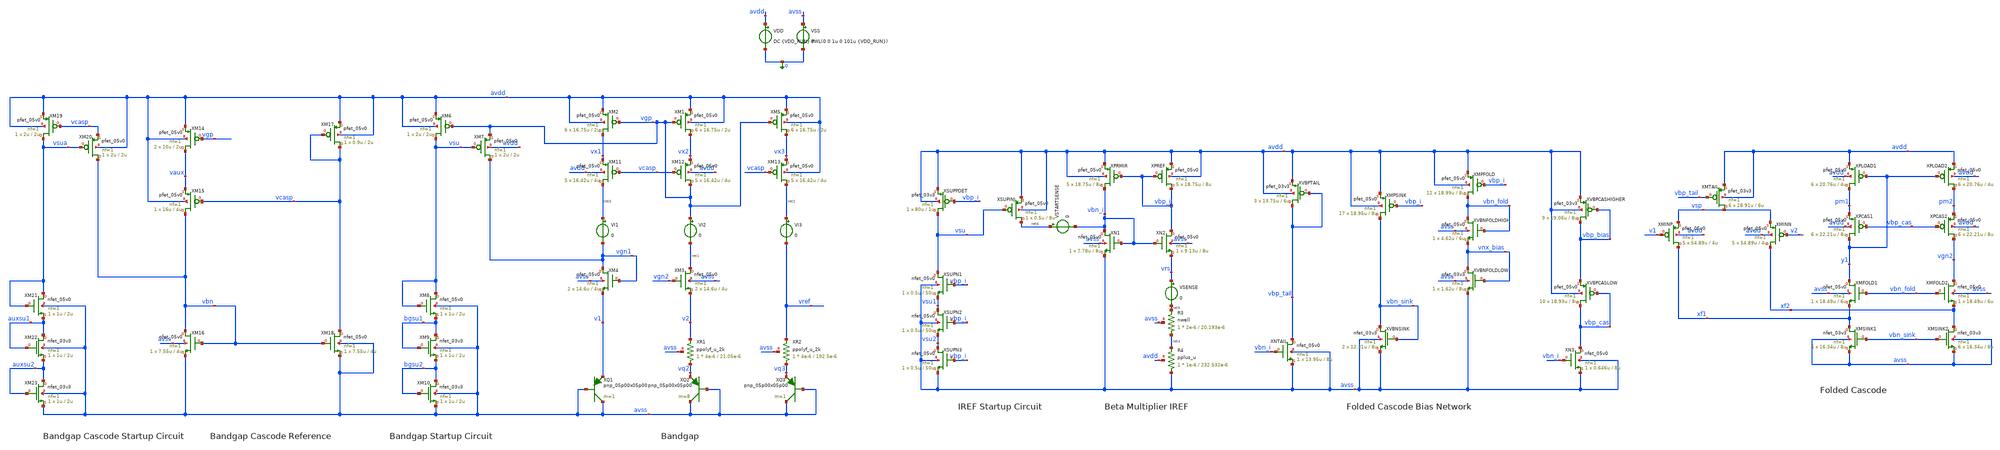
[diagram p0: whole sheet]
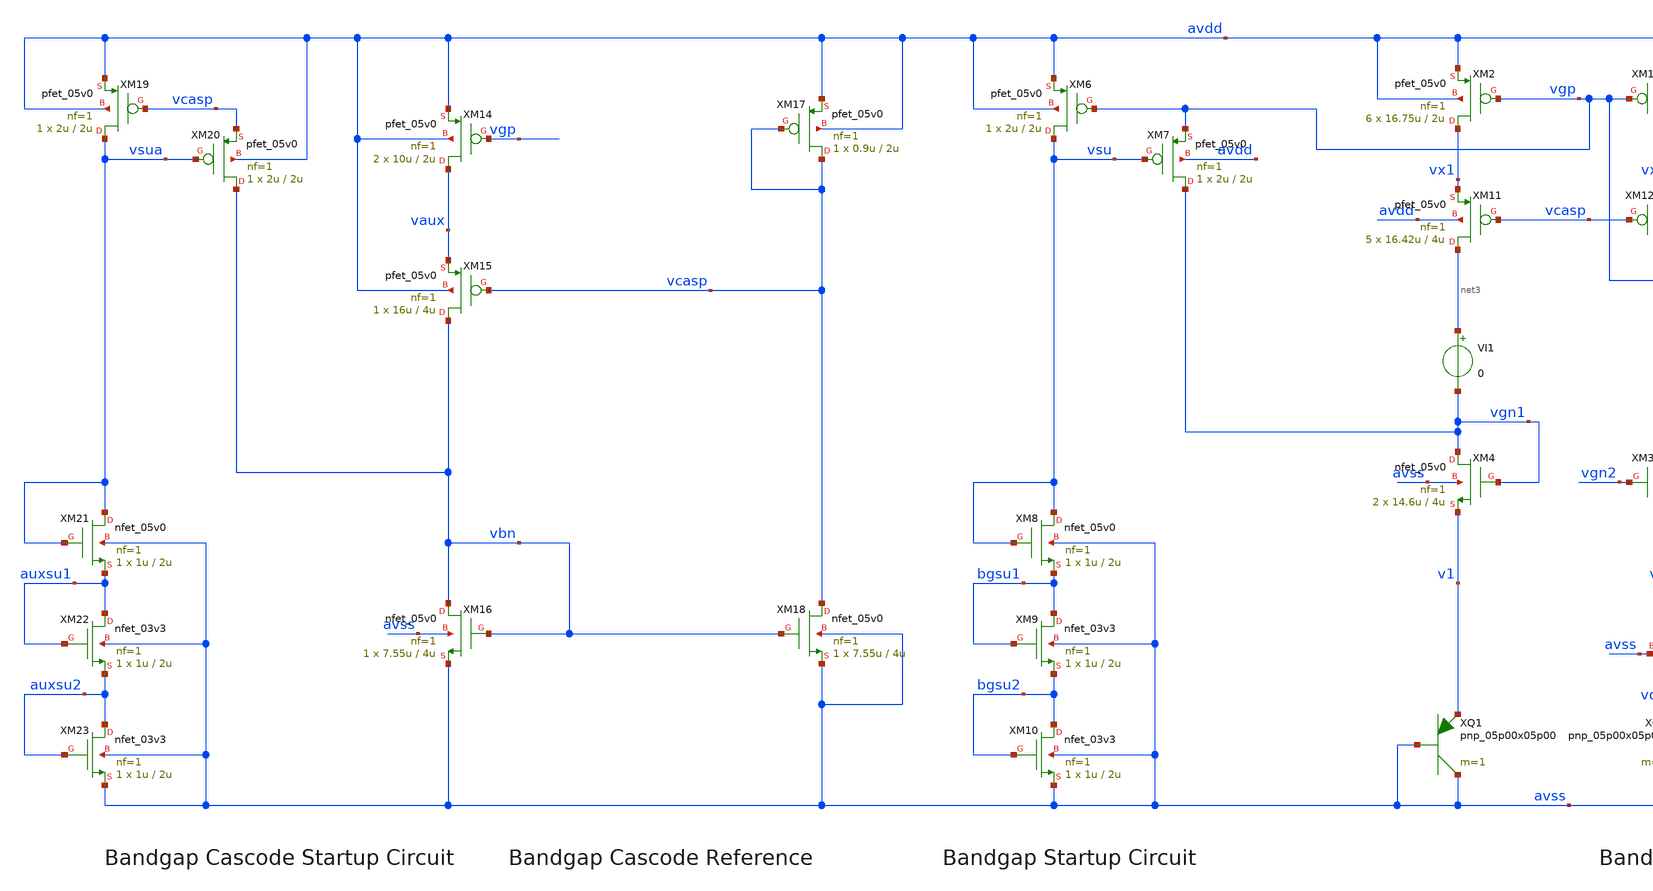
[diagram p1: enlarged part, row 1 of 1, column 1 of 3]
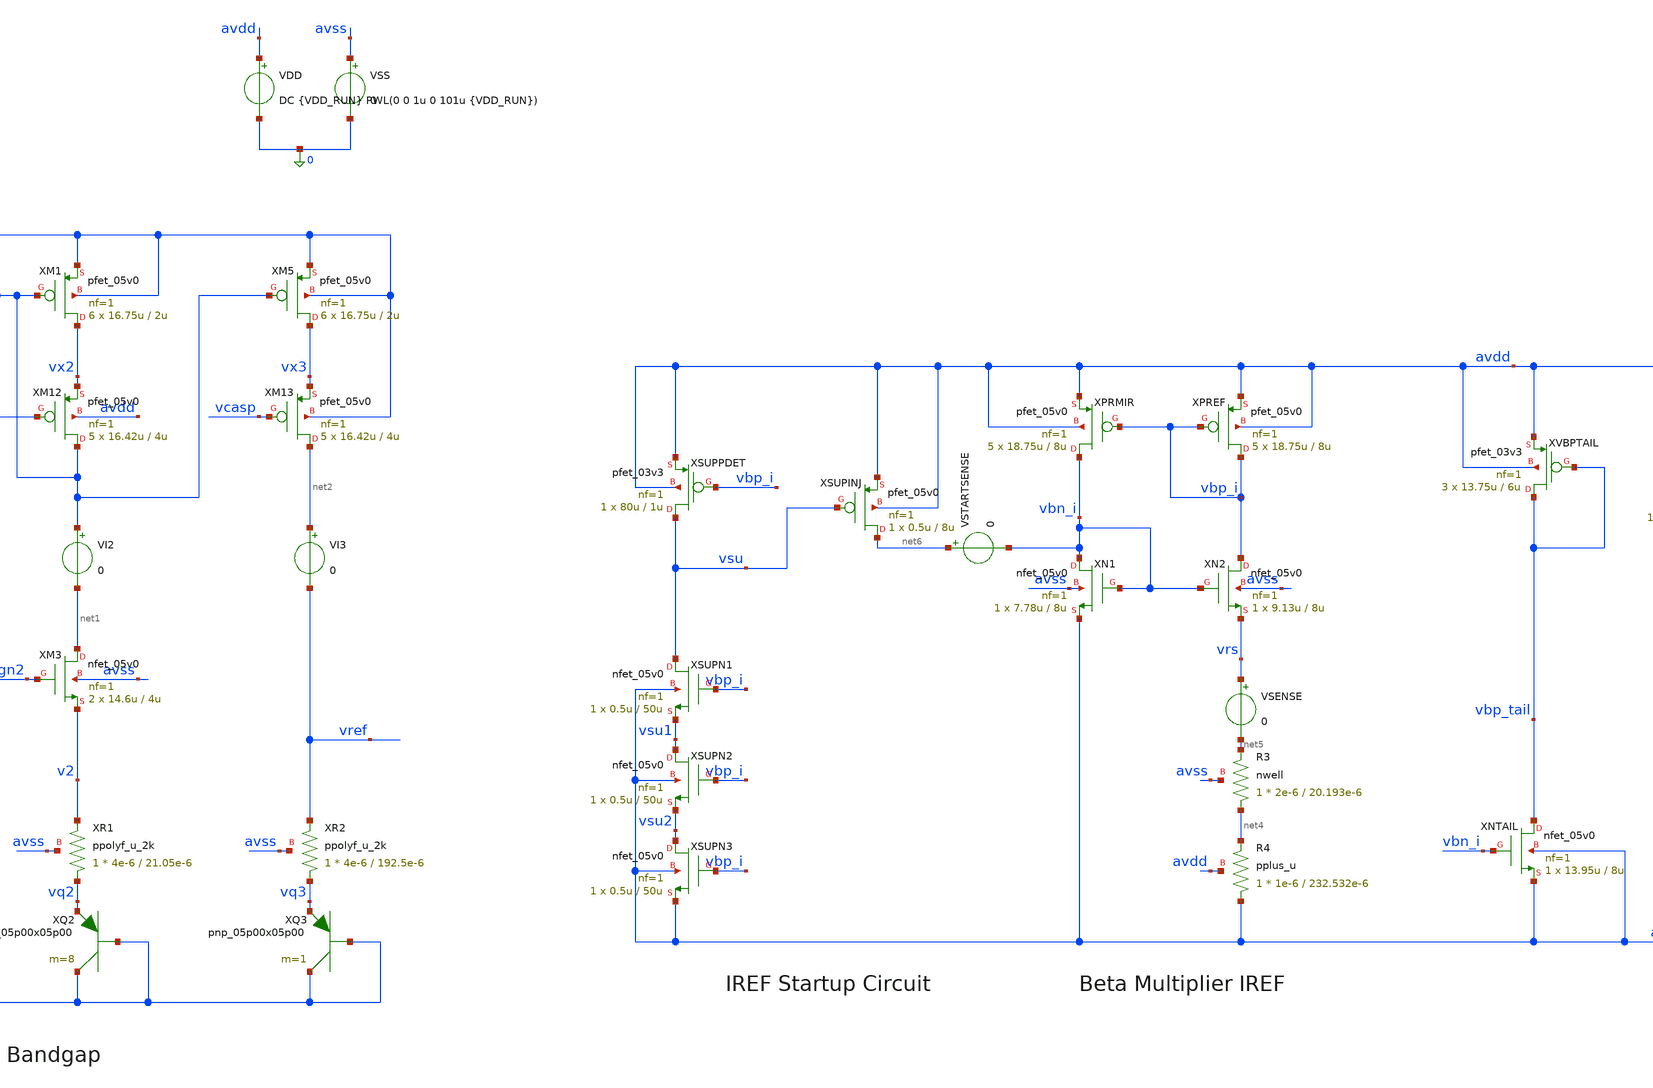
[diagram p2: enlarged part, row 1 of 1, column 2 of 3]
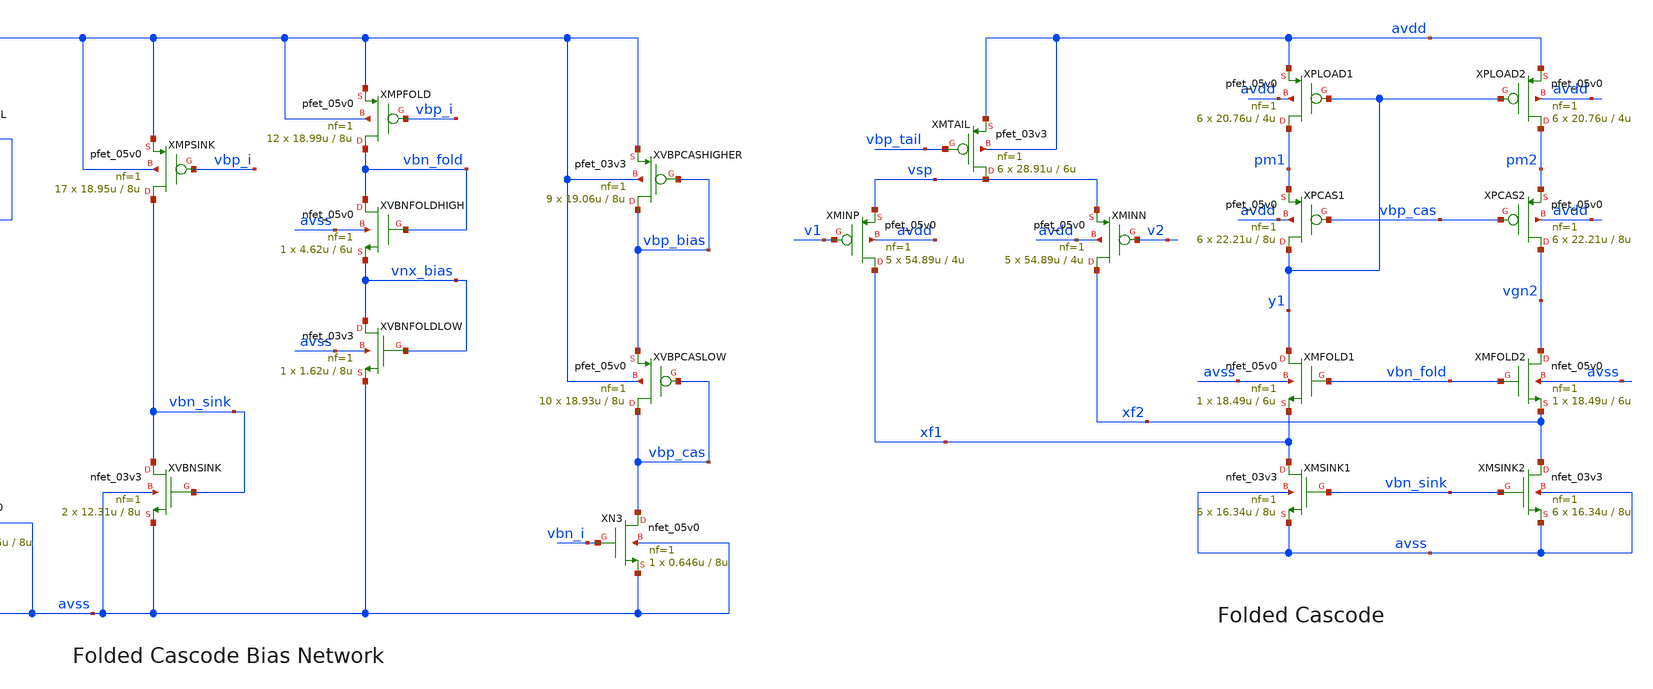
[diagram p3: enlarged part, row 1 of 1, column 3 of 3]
** sch_path: examples/gf180-bandgap/5vfullv2-startup.sch
**.subckt 5vfullv2-startup
XQ3 avss avss vq3 pnp_05p00x05p00 m=1
XQ2 avss avss vq2 pnp_05p00x05p00 m=8
XQ1 avss avss v1 pnp_05p00x05p00 m=1
XM9 bgsu1 bgsu1 bgsu2 avss nfet_03v3 L=2u W=1u nf=1 ad='int((nf+1)/2) * W/nf * 0.18u' as='int((nf+2)/2) * W/nf * 0.18u'
+ pd='2*int((nf+1)/2) * (W/nf + 0.18u)' ps='2*int((nf+2)/2) * (W/nf + 0.18u)' nrd='0.18u / W' nrs='0.18u / W'
+ sa=0 sb=0 sd=0 m=1
XM10 bgsu2 bgsu2 avss avss nfet_03v3 L=2u W=1u nf=1 ad='int((nf+1)/2) * W/nf * 0.18u' as='int((nf+2)/2) * W/nf * 0.18u'
+ pd='2*int((nf+1)/2) * (W/nf + 0.18u)' ps='2*int((nf+2)/2) * (W/nf + 0.18u)' nrd='0.18u / W' nrs='0.18u / W'
+ sa=0 sb=0 sd=0 m=1
XR1 vq2 v2 avss ppolyf_u_2k r_width=4e-6 r_length=21.05e-6 m=1
XR2 vq3 vref avss ppolyf_u_2k r_width=4e-6 r_length=192.5e-6 m=1
VI1 net3 vgn1 0
VI2 vgp net1 0
VI3 net2 vref 0
XM22 auxsu1 auxsu1 auxsu2 avss nfet_03v3 L=2u W=1u nf=1 ad='int((nf+1)/2) * W/nf * 0.18u' as='int((nf+2)/2) * W/nf * 0.18u'
+ pd='2*int((nf+1)/2) * (W/nf + 0.18u)' ps='2*int((nf+2)/2) * (W/nf + 0.18u)' nrd='0.18u / W' nrs='0.18u / W'
+ sa=0 sb=0 sd=0 m=1
XM23 auxsu2 auxsu2 avss avss nfet_03v3 L=2u W=1u nf=1 ad='int((nf+1)/2) * W/nf * 0.18u' as='int((nf+2)/2) * W/nf * 0.18u'
+ pd='2*int((nf+1)/2) * (W/nf + 0.18u)' ps='2*int((nf+2)/2) * (W/nf + 0.18u)' nrd='0.18u / W' nrs='0.18u / W'
+ sa=0 sb=0 sd=0 m=1
XMTAIL vsp vbp_tail avdd avdd pfet_03v3 L=6u W=28.91u nf=1 ad='int((nf+1)/2) * W/nf * 0.18u' as='int((nf+2)/2) * W/nf * 0.18u'
+ pd='2*int((nf+1)/2) * (W/nf + 0.18u)' ps='2*int((nf+2)/2) * (W/nf + 0.18u)' nrd='0.18u / W' nrs='0.18u / W'
+ sa=0 sb=0 sd=0 m=6
VDD avdd 0 DC {VDD_RUN} PWL(0 0 1u 0 101u {VDD_RUN})
VSS avss 0 0
XMSINK1 xf1 vbn_sink avss avss nfet_03v3 L=8u W=16.34u nf=1 ad='int((nf+1)/2) * W/nf * 0.18u' as='int((nf+2)/2) * W/nf * 0.18u'
+ pd='2*int((nf+1)/2) * (W/nf + 0.18u)' ps='2*int((nf+2)/2) * (W/nf + 0.18u)' nrd='0.18u / W' nrs='0.18u / W'
+ sa=0 sb=0 sd=0 m=6
XMSINK2 xf2 vbn_sink avss avss nfet_03v3 L=8u W=16.34u nf=1 ad='int((nf+1)/2) * W/nf * 0.18u' as='int((nf+2)/2) * W/nf * 0.18u'
+ pd='2*int((nf+1)/2) * (W/nf + 0.18u)' ps='2*int((nf+2)/2) * (W/nf + 0.18u)' nrd='0.18u / W' nrs='0.18u / W'
+ sa=0 sb=0 sd=0 m=6
XR3 net4 net5 avss nwell r_width=2e-6 r_length=20.193e-6 m=1
XR4 avss net4 avdd pplus_u r_width=1e-6 r_length=232.532e-6 m=1
VSENSE vrs net5 0
XSUPPDET vsu vbp_i avdd avdd pfet_03v3 L=1u W=80u nf=1 ad='int((nf+1)/2) * W/nf * 0.18u' as='int((nf+2)/2) * W/nf * 0.18u'
+ pd='2*int((nf+1)/2) * (W/nf + 0.18u)' ps='2*int((nf+2)/2) * (W/nf + 0.18u)' nrd='0.18u / W' nrs='0.18u / W'
+ sa=0 sb=0 sd=0 m=1
VSTARTSENSE net6 vbn_i 0
XPCAS2 vgn2 vbp_cas pm2 avdd pfet_05v0 L=8u W=22.21u nf=1 ad='int((nf+1)/2) * W/nf * 0.18u' as='int((nf+2)/2) * W/nf * 0.18u'
+ pd='2*int((nf+1)/2) * (W/nf + 0.18u)' ps='2*int((nf+2)/2) * (W/nf + 0.18u)' nrd='0.18u / W' nrs='0.18u / W'
+ sa=0 sb=0 sd=0 m=6
XPCAS1 y1 vbp_cas pm1 avdd pfet_05v0 L=8u W=22.21u nf=1 ad='int((nf+1)/2) * W/nf * 0.18u' as='int((nf+2)/2) * W/nf * 0.18u'
+ pd='2*int((nf+1)/2) * (W/nf + 0.18u)' ps='2*int((nf+2)/2) * (W/nf + 0.18u)' nrd='0.18u / W' nrs='0.18u / W'
+ sa=0 sb=0 sd=0 m=6
XMINN xf2 v2 vsp avdd pfet_05v0 L=4u W=54.89u nf=1 ad='int((nf+1)/2) * W/nf * 0.18u' as='int((nf+2)/2) * W/nf * 0.18u'
+ pd='2*int((nf+1)/2) * (W/nf + 0.18u)' ps='2*int((nf+2)/2) * (W/nf + 0.18u)' nrd='0.18u / W' nrs='0.18u / W'
+ sa=0 sb=0 sd=0 m=5
XMINP xf1 v1 vsp avdd pfet_05v0 L=4u W=54.89u nf=1 ad='int((nf+1)/2) * W/nf * 0.18u' as='int((nf+2)/2) * W/nf * 0.18u'
+ pd='2*int((nf+1)/2) * (W/nf + 0.18u)' ps='2*int((nf+2)/2) * (W/nf + 0.18u)' nrd='0.18u / W' nrs='0.18u / W'
+ sa=0 sb=0 sd=0 m=5
XMFOLD2 vgn2 vbn_fold xf2 avss nfet_05v0 L=6u W=18.49u nf=1 ad='int((nf+1)/2) * W/nf * 0.18u' as='int((nf+2)/2) * W/nf * 0.18u'
+ pd='2*int((nf+1)/2) * (W/nf + 0.18u)' ps='2*int((nf+2)/2) * (W/nf + 0.18u)' nrd='0.18u / W' nrs='0.18u / W'
+ sa=0 sb=0 sd=0 m=1
XMFOLD1 y1 vbn_fold xf1 avss nfet_05v0 L=6u W=18.49u nf=1 ad='int((nf+1)/2) * W/nf * 0.18u' as='int((nf+2)/2) * W/nf * 0.18u'
+ pd='2*int((nf+1)/2) * (W/nf + 0.18u)' ps='2*int((nf+2)/2) * (W/nf + 0.18u)' nrd='0.18u / W' nrs='0.18u / W'
+ sa=0 sb=0 sd=0 m=1
XN1 vbn_i vbn_i avss avss nfet_05v0 L=8u W=7.78u nf=1 ad='int((nf+1)/2) * W/nf * 0.18u' as='int((nf+2)/2) * W/nf * 0.18u'
+ pd='2*int((nf+1)/2) * (W/nf + 0.18u)' ps='2*int((nf+2)/2) * (W/nf + 0.18u)' nrd='0.18u / W' nrs='0.18u / W'
+ sa=0 sb=0 sd=0 m=1
XN2 vbp_i vbn_i vrs avss nfet_05v0 L=8u W=9.13u nf=1 ad='int((nf+1)/2) * W/nf * 0.18u' as='int((nf+2)/2) * W/nf * 0.18u'
+ pd='2*int((nf+1)/2) * (W/nf + 0.18u)' ps='2*int((nf+2)/2) * (W/nf + 0.18u)' nrd='0.18u / W' nrs='0.18u / W'
+ sa=0 sb=0 sd=0 m=1
XPREF vbp_i vbp_i avdd avdd pfet_05v0 L=8u W=18.75u nf=1 ad='int((nf+1)/2) * W/nf * 0.18u' as='int((nf+2)/2) * W/nf * 0.18u'
+ pd='2*int((nf+1)/2) * (W/nf + 0.18u)' ps='2*int((nf+2)/2) * (W/nf + 0.18u)' nrd='0.18u / W' nrs='0.18u / W'
+ sa=0 sb=0 sd=0 m=5
XPRMIR vbn_i vbp_i avdd avdd pfet_05v0 L=8u W=18.75u nf=1 ad='int((nf+1)/2) * W/nf * 0.18u' as='int((nf+2)/2) * W/nf * 0.18u'
+ pd='2*int((nf+1)/2) * (W/nf + 0.18u)' ps='2*int((nf+2)/2) * (W/nf + 0.18u)' nrd='0.18u / W' nrs='0.18u / W'
+ sa=0 sb=0 sd=0 m=5
XNTAIL vbp_tail vbn_i avss avss nfet_05v0 L=8u W=13.95u nf=1 ad='int((nf+1)/2) * W/nf * 0.18u' as='int((nf+2)/2) * W/nf * 0.18u'
+ pd='2*int((nf+1)/2) * (W/nf + 0.18u)' ps='2*int((nf+2)/2) * (W/nf + 0.18u)' nrd='0.18u / W' nrs='0.18u / W'
+ sa=0 sb=0 sd=0 m=1
XN3 vbp_cas vbn_i avss avss nfet_05v0 L=8u W=0.646u nf=1 ad='int((nf+1)/2) * W/nf * 0.18u' as='int((nf+2)/2) * W/nf * 0.18u'
+ pd='2*int((nf+1)/2) * (W/nf + 0.18u)' ps='2*int((nf+2)/2) * (W/nf + 0.18u)' nrd='0.18u / W' nrs='0.18u / W'
+ sa=0 sb=0 sd=0 m=1
XMPSINK vbn_sink vbp_i avdd avdd pfet_05v0 L=8u W=18.95u nf=1 ad='int((nf+1)/2) * W/nf * 0.18u' as='int((nf+2)/2) * W/nf * 0.18u'
+ pd='2*int((nf+1)/2) * (W/nf + 0.18u)' ps='2*int((nf+2)/2) * (W/nf + 0.18u)' nrd='0.18u / W' nrs='0.18u / W'
+ sa=0 sb=0 sd=0 m=17
XMPFOLD vbn_fold vbp_i avdd avdd pfet_05v0 L=8u W=18.99u nf=1 ad='int((nf+1)/2) * W/nf * 0.18u' as='int((nf+2)/2) * W/nf * 0.18u'
+ pd='2*int((nf+1)/2) * (W/nf + 0.18u)' ps='2*int((nf+2)/2) * (W/nf + 0.18u)' nrd='0.18u / W' nrs='0.18u / W'
+ sa=0 sb=0 sd=0 m=12
XVBNFOLDHIGH vbn_fold vbn_fold vnx_bias avss nfet_05v0 L=6u W=4.62u nf=1 ad='int((nf+1)/2) * W/nf * 0.18u'
+ as='int((nf+2)/2) * W/nf * 0.18u' pd='2*int((nf+1)/2) * (W/nf + 0.18u)' ps='2*int((nf+2)/2) * (W/nf + 0.18u)'
+ nrd='0.18u / W' nrs='0.18u / W' sa=0 sb=0 sd=0 m=1
XVBPCASLOW vbp_cas vbp_cas vbp_bias avdd pfet_05v0 L=8u W=18.93u nf=1 ad='int((nf+1)/2) * W/nf * 0.18u'
+ as='int((nf+2)/2) * W/nf * 0.18u' pd='2*int((nf+1)/2) * (W/nf + 0.18u)' ps='2*int((nf+2)/2) * (W/nf + 0.18u)'
+ nrd='0.18u / W' nrs='0.18u / W' sa=0 sb=0 sd=0 m=10
XVBNSINK vbn_sink vbn_sink avss avss nfet_03v3 L=8u W=12.31u nf=1 ad='int((nf+1)/2) * W/nf * 0.18u' as='int((nf+2)/2) * W/nf * 0.18u'
+ pd='2*int((nf+1)/2) * (W/nf + 0.18u)' ps='2*int((nf+2)/2) * (W/nf + 0.18u)' nrd='0.18u / W' nrs='0.18u / W'
+ sa=0 sb=0 sd=0 m=2
XVBPTAIL vbp_tail vbp_tail avdd avdd pfet_03v3 L=6u W=13.75u nf=1 ad='int((nf+1)/2) * W/nf * 0.18u' as='int((nf+2)/2) * W/nf * 0.18u'
+ pd='2*int((nf+1)/2) * (W/nf + 0.18u)' ps='2*int((nf+2)/2) * (W/nf + 0.18u)' nrd='0.18u / W' nrs='0.18u / W'
+ sa=0 sb=0 sd=0 m=3
XVBNFOLDLOW vnx_bias vnx_bias avss avss nfet_03v3 L=8u W=1.62u nf=1 ad='int((nf+1)/2) * W/nf * 0.18u'
+ as='int((nf+2)/2) * W/nf * 0.18u' pd='2*int((nf+1)/2) * (W/nf + 0.18u)' ps='2*int((nf+2)/2) * (W/nf + 0.18u)'
+ nrd='0.18u / W' nrs='0.18u / W' sa=0 sb=0 sd=0 m=1
XVBPCASHIGHER vbp_bias vbp_bias avdd avdd pfet_03v3 L=8u W=19.06u nf=1 ad='int((nf+1)/2) * W/nf * 0.18u'
+ as='int((nf+2)/2) * W/nf * 0.18u' pd='2*int((nf+1)/2) * (W/nf + 0.18u)' ps='2*int((nf+2)/2) * (W/nf + 0.18u)'
+ nrd='0.18u / W' nrs='0.18u / W' sa=0 sb=0 sd=0 m=9
XSUPN1 vsu vbp_i vsu1 avss nfet_05v0 L=50u W=0.5u nf=1 ad='int((nf+1)/2) * W/nf * 0.18u' as='int((nf+2)/2) * W/nf * 0.18u'
+ pd='2*int((nf+1)/2) * (W/nf + 0.18u)' ps='2*int((nf+2)/2) * (W/nf + 0.18u)' nrd='0.18u / W' nrs='0.18u / W'
+ sa=0 sb=0 sd=0 m=1
XSUPN2 vsu1 vbp_i vsu2 avss nfet_05v0 L=50u W=0.5u nf=1 ad='int((nf+1)/2) * W/nf * 0.18u' as='int((nf+2)/2) * W/nf * 0.18u'
+ pd='2*int((nf+1)/2) * (W/nf + 0.18u)' ps='2*int((nf+2)/2) * (W/nf + 0.18u)' nrd='0.18u / W' nrs='0.18u / W'
+ sa=0 sb=0 sd=0 m=1
XSUPN3 vsu2 vbp_i avss avss nfet_05v0 L=50u W=0.5u nf=1 ad='int((nf+1)/2) * W/nf * 0.18u' as='int((nf+2)/2) * W/nf * 0.18u'
+ pd='2*int((nf+1)/2) * (W/nf + 0.18u)' ps='2*int((nf+2)/2) * (W/nf + 0.18u)' nrd='0.18u / W' nrs='0.18u / W'
+ sa=0 sb=0 sd=0 m=1
XSUPINJ net6 vsu avdd avdd pfet_05v0 L=8u W=0.5u nf=1 ad='int((nf+1)/2) * W/nf * 0.18u' as='int((nf+2)/2) * W/nf * 0.18u'
+ pd='2*int((nf+1)/2) * (W/nf + 0.18u)' ps='2*int((nf+2)/2) * (W/nf + 0.18u)' nrd='0.18u / W' nrs='0.18u / W'
+ sa=0 sb=0 sd=0 m=1
XM11 net3 vcasp vx1 avdd pfet_05v0 L=4u W=16.42u nf=1 ad='int((nf+1)/2) * W/nf * 0.18u' as='int((nf+2)/2) * W/nf * 0.18u'
+ pd='2*int((nf+1)/2) * (W/nf + 0.18u)' ps='2*int((nf+2)/2) * (W/nf + 0.18u)' nrd='0.18u / W' nrs='0.18u / W'
+ sa=0 sb=0 sd=0 m=5
XM12 vgp vcasp vx2 avdd pfet_05v0 L=4u W=16.42u nf=1 ad='int((nf+1)/2) * W/nf * 0.18u' as='int((nf+2)/2) * W/nf * 0.18u'
+ pd='2*int((nf+1)/2) * (W/nf + 0.18u)' ps='2*int((nf+2)/2) * (W/nf + 0.18u)' nrd='0.18u / W' nrs='0.18u / W'
+ sa=0 sb=0 sd=0 m=5
XM13 net2 vcasp vx3 avdd pfet_05v0 L=4u W=16.42u nf=1 ad='int((nf+1)/2) * W/nf * 0.18u' as='int((nf+2)/2) * W/nf * 0.18u'
+ pd='2*int((nf+1)/2) * (W/nf + 0.18u)' ps='2*int((nf+2)/2) * (W/nf + 0.18u)' nrd='0.18u / W' nrs='0.18u / W'
+ sa=0 sb=0 sd=0 m=5
XM4 vgn1 vgn1 v1 avss nfet_05v0 L=4u W=14.6u nf=1 ad='int((nf+1)/2) * W/nf * 0.18u' as='int((nf+2)/2) * W/nf * 0.18u'
+ pd='2*int((nf+1)/2) * (W/nf + 0.18u)' ps='2*int((nf+2)/2) * (W/nf + 0.18u)' nrd='0.18u / W' nrs='0.18u / W'
+ sa=0 sb=0 sd=0 m=2
XM3 net1 vgn2 v2 avss nfet_05v0 L=4u W=14.6u nf=1 ad='int((nf+1)/2) * W/nf * 0.18u' as='int((nf+2)/2) * W/nf * 0.18u'
+ pd='2*int((nf+1)/2) * (W/nf + 0.18u)' ps='2*int((nf+2)/2) * (W/nf + 0.18u)' nrd='0.18u / W' nrs='0.18u / W'
+ sa=0 sb=0 sd=0 m=2
XM16 vbn vbn avss avss nfet_05v0 L=4u W=7.55u nf=1 ad='int((nf+1)/2) * W/nf * 0.18u' as='int((nf+2)/2) * W/nf * 0.18u'
+ pd='2*int((nf+1)/2) * (W/nf + 0.18u)' ps='2*int((nf+2)/2) * (W/nf + 0.18u)' nrd='0.18u / W' nrs='0.18u / W'
+ sa=0 sb=0 sd=0 m=1
XM18 vcasp vbn avss avss nfet_05v0 L=4u W=7.55u nf=1 ad='int((nf+1)/2) * W/nf * 0.18u' as='int((nf+2)/2) * W/nf * 0.18u'
+ pd='2*int((nf+1)/2) * (W/nf + 0.18u)' ps='2*int((nf+2)/2) * (W/nf + 0.18u)' nrd='0.18u / W' nrs='0.18u / W'
+ sa=0 sb=0 sd=0 m=1
XM15 vbn vcasp vaux avdd pfet_05v0 L=4u W=16u nf=1 ad='int((nf+1)/2) * W/nf * 0.18u' as='int((nf+2)/2) * W/nf * 0.18u'
+ pd='2*int((nf+1)/2) * (W/nf + 0.18u)' ps='2*int((nf+2)/2) * (W/nf + 0.18u)' nrd='0.18u / W' nrs='0.18u / W'
+ sa=0 sb=0 sd=0 m=1
XM17 vcasp vcasp avdd avdd pfet_05v0 L=2u W=0.9u nf=1 ad='int((nf+1)/2) * W/nf * 0.18u' as='int((nf+2)/2) * W/nf * 0.18u'
+ pd='2*int((nf+1)/2) * (W/nf + 0.18u)' ps='2*int((nf+2)/2) * (W/nf + 0.18u)' nrd='0.18u / W' nrs='0.18u / W'
+ sa=0 sb=0 sd=0 m=1
XM6 vsu vgp avdd avdd pfet_05v0 L=2u W=2u nf=1 ad='int((nf+1)/2) * W/nf * 0.18u' as='int((nf+2)/2) * W/nf * 0.18u'
+ pd='2*int((nf+1)/2) * (W/nf + 0.18u)' ps='2*int((nf+2)/2) * (W/nf + 0.18u)' nrd='0.18u / W' nrs='0.18u / W'
+ sa=0 sb=0 sd=0 m=1
XM7 vgn1 vsu vgp avdd pfet_05v0 L=2u W=2u nf=1 ad='int((nf+1)/2) * W/nf * 0.18u' as='int((nf+2)/2) * W/nf * 0.18u'
+ pd='2*int((nf+1)/2) * (W/nf + 0.18u)' ps='2*int((nf+2)/2) * (W/nf + 0.18u)' nrd='0.18u / W' nrs='0.18u / W'
+ sa=0 sb=0 sd=0 m=1
XM19 vsua vcasp avdd avdd pfet_05v0 L=2u W=2u nf=1 ad='int((nf+1)/2) * W/nf * 0.18u' as='int((nf+2)/2) * W/nf * 0.18u'
+ pd='2*int((nf+1)/2) * (W/nf + 0.18u)' ps='2*int((nf+2)/2) * (W/nf + 0.18u)' nrd='0.18u / W' nrs='0.18u / W'
+ sa=0 sb=0 sd=0 m=1
XM20 vbn vsua vcasp avdd pfet_05v0 L=2u W=2u nf=1 ad='int((nf+1)/2) * W/nf * 0.18u' as='int((nf+2)/2) * W/nf * 0.18u'
+ pd='2*int((nf+1)/2) * (W/nf + 0.18u)' ps='2*int((nf+2)/2) * (W/nf + 0.18u)' nrd='0.18u / W' nrs='0.18u / W'
+ sa=0 sb=0 sd=0 m=1
XM8 vsu vsu bgsu1 avss nfet_05v0 L=2u W=1u nf=1 ad='int((nf+1)/2) * W/nf * 0.18u' as='int((nf+2)/2) * W/nf * 0.18u'
+ pd='2*int((nf+1)/2) * (W/nf + 0.18u)' ps='2*int((nf+2)/2) * (W/nf + 0.18u)' nrd='0.18u / W' nrs='0.18u / W'
+ sa=0 sb=0 sd=0 m=1
XM21 vsua vsua auxsu1 avss nfet_05v0 L=2u W=1u nf=1 ad='int((nf+1)/2) * W/nf * 0.18u' as='int((nf+2)/2) * W/nf * 0.18u'
+ pd='2*int((nf+1)/2) * (W/nf + 0.18u)' ps='2*int((nf+2)/2) * (W/nf + 0.18u)' nrd='0.18u / W' nrs='0.18u / W'
+ sa=0 sb=0 sd=0 m=1
XPLOAD1 pm1 y1 avdd avdd pfet_05v0 L=4u W=20.76u nf=1 ad='int((nf+1)/2) * W/nf * 0.18u' as='int((nf+2)/2) * W/nf * 0.18u'
+ pd='2*int((nf+1)/2) * (W/nf + 0.18u)' ps='2*int((nf+2)/2) * (W/nf + 0.18u)' nrd='0.18u / W' nrs='0.18u / W'
+ sa=0 sb=0 sd=0 m=6
XPLOAD2 pm2 y1 avdd avdd pfet_05v0 L=4u W=20.76u nf=1 ad='int((nf+1)/2) * W/nf * 0.18u' as='int((nf+2)/2) * W/nf * 0.18u'
+ pd='2*int((nf+1)/2) * (W/nf + 0.18u)' ps='2*int((nf+2)/2) * (W/nf + 0.18u)' nrd='0.18u / W' nrs='0.18u / W'
+ sa=0 sb=0 sd=0 m=6
XM2 vx1 vgp avdd avdd pfet_05v0 L=2u W=16.75u nf=1 ad='int((nf+1)/2) * W/nf * 0.18u' as='int((nf+2)/2) * W/nf * 0.18u'
+ pd='2*int((nf+1)/2) * (W/nf + 0.18u)' ps='2*int((nf+2)/2) * (W/nf + 0.18u)' nrd='0.18u / W' nrs='0.18u / W'
+ sa=0 sb=0 sd=0 m=6
XM1 vx2 vgp avdd avdd pfet_05v0 L=2u W=16.75u nf=1 ad='int((nf+1)/2) * W/nf * 0.18u' as='int((nf+2)/2) * W/nf * 0.18u'
+ pd='2*int((nf+1)/2) * (W/nf + 0.18u)' ps='2*int((nf+2)/2) * (W/nf + 0.18u)' nrd='0.18u / W' nrs='0.18u / W'
+ sa=0 sb=0 sd=0 m=6
XM5 vx3 vgp avdd avdd pfet_05v0 L=2u W=16.75u nf=1 ad='int((nf+1)/2) * W/nf * 0.18u' as='int((nf+2)/2) * W/nf * 0.18u'
+ pd='2*int((nf+1)/2) * (W/nf + 0.18u)' ps='2*int((nf+2)/2) * (W/nf + 0.18u)' nrd='0.18u / W' nrs='0.18u / W'
+ sa=0 sb=0 sd=0 m=6
XM14 vaux vgp avdd avdd pfet_05v0 L=2u W=10u nf=1 ad='int((nf+1)/2) * W/nf * 0.18u' as='int((nf+2)/2) * W/nf * 0.18u'
+ pd='2*int((nf+1)/2) * (W/nf + 0.18u)' ps='2*int((nf+2)/2) * (W/nf + 0.18u)' nrd='0.18u / W' nrs='0.18u / W'
+ sa=0 sb=0 sd=0 m=2
**** begin user architecture code

* =====================================================================
* GF180 BANDGAP — FULL CHARACTERIZATION V5, 5-V-CAPABLE LOW-TC CORE
*
* Basis:
*   - latest cumulative handoff
*   - full2/full-characterization testbench structure
*   - current accepted rounded MOS geometry
*   - low-TC resistor point XR1=21.05 um, XR2=192.50 um
*
* REQUIRED FUNCTIONAL RANGE:
*   VDD = 3.0 to 5.0 V
*   T   = -40 to 125 C
*
* ROBUSTNESS ONLY:
*   VDD = 5.5 V
*
* WORKING SPEC TARGETS:
*   VREF            1.194 / 1.200 / 1.206 V
*   initial accuracy +/-0.5 %
*   IDD              20 / 30 / 50 uA  (project interpretation still open)
*   line regulation  0.01 / 0.05 / 0.1 % (endpoint interpretation used)
*   PSRR             60 / 70 / 80 dB   (frequency not yet specified)
*   noise            20 / 50 / 100 nV/sqrt(Hz) (frequency not yet specified)
*   TC               10 / 20 / 30 ppm/C
*   startup          50 / 100 / 200 us
*   IREF             180 / 220 / 260 nA
*
* IMPORTANT METHODOLOGY:
*   - clean DC/temp/line characterization uses fresh reset -> direct dc.
*   - no transient or op is allowed before authoritative clean DC sweeps.
*   - startup is characterized with a real supply ramp from 0 V.
*   - final startup leakage is SIGNED avg(i(VSTARTSENSE)).
*   - 5.5 V is reported separately and is not included in required-range
*     optimization/pass-fail.
*   - load tests are diagnostic only because no final load spec exists.
*   - output noise is intentionally in a separate validated-minimal deck.
*   - process corners are separate because .lib sections are parse-time.
*   - integrated loop gain is separate because the loop-break location must
*     be explicitly inserted/validated; do not infer PM from standalone OTA.
*
* OUTPUT DIRECTORY:
*   /foss/designs/chipalooza-bandgap/full_characterization_v5_5v
* =====================================================================

.include /foss/pdks/gf180mcuD/libs.tech/ngspice/design.ngspice
.lib /foss/pdks/gf180mcuD/libs.tech/ngspice/sm141064.ngspice typical
.lib /foss/pdks/gf180mcuD/libs.tech/ngspice/sm141064.ngspice bjt_typical
.lib /foss/pdks/gf180mcuD/libs.tech/ngspice/sm141064.ngspice res_typical

.options tnom=25

.param sw_stat_global=0
.param sw_stat_mismatch=0
.param fnoicor=0

* Current low-TC resistor target.  These parameters are documentary if the
* schematic uses fixed physical lengths.
.param XR1_L_UM=21.05
.param XR2_L_UM=192.50

.param VDD_RUN=5.0
.param P_ILOAD_DC=0
.param P_ILOAD_STEP=0
.param P_ZAC=0

* Testbench-only loads/injection.
ITBLOADDC   vref 0 DC {P_ILOAD_DC}
ITBLOADSTEP vref 0 PWL(0 0 2m 0 2001u {P_ILOAD_STEP} 2500u {P_ILOAD_STEP} 2501u 0)
ITBZ        vref 0 DC 0 AC {P_ZAC}

.control
set noaskquit
set temp=25
save all
tran 100n 3m
meas tran vref_final avg v(vref) from=2800u to=3000u
meas tran supply_final avg v(avdd) from=2800u to=3000u
.endc


**** end user architecture code
**.ends
.end
